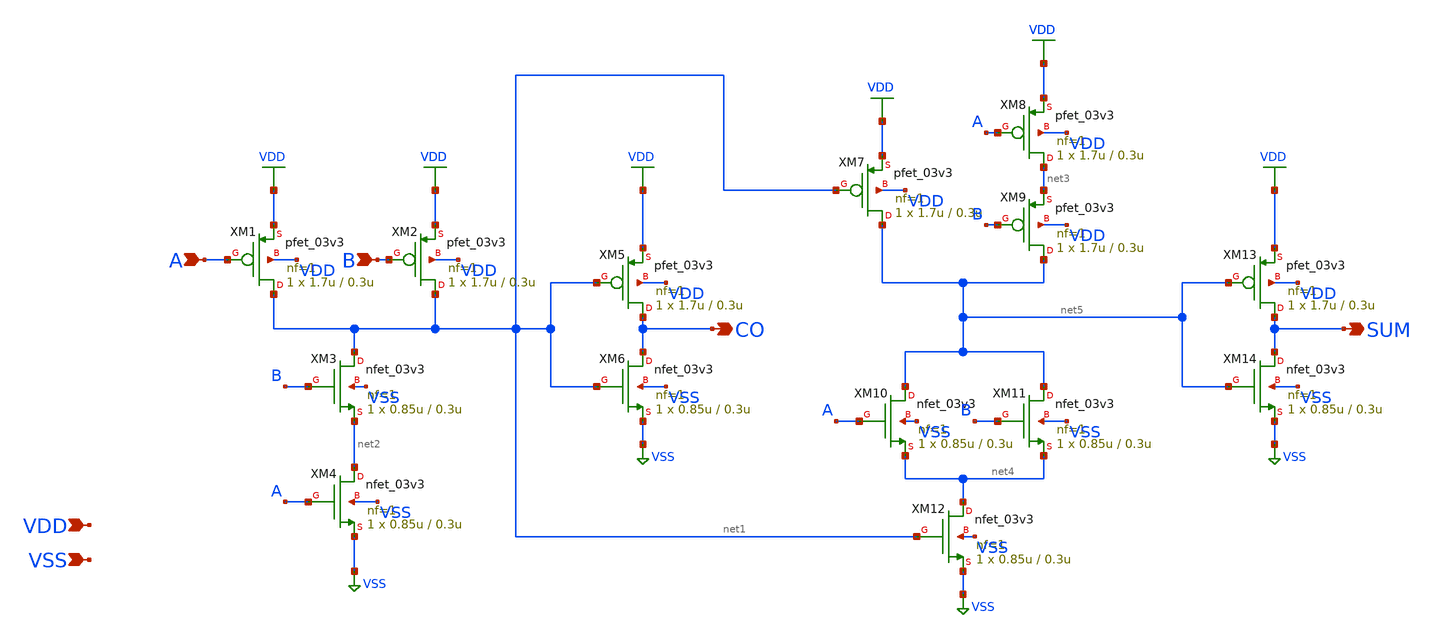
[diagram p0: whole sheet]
** sch_path: gf180mcu_osu_sc_gp9t3v3/xschem/gf180mcu_osu_sc_gp9t3v3__addh_1.sch
**.subckt gf180mcu_osu_sc_gp9t3v3__addh_1 A B SUM CO VDD VSS
*.ipin A
*.ipin B
*.opin SUM
*.opin CO
*.ipin VDD
*.ipin VSS
XM1 net1 A VDD VDD pfet_03v3 L=0.3u W=1.7u nf=1 ad='int((nf+1)/2) * W/nf * 0.18u' as='int((nf+2)/2) * W/nf * 0.18u'
+ pd='2*int((nf+1)/2) * (W/nf + 0.18u)' ps='2*int((nf+2)/2) * (W/nf + 0.18u)' nrd='0.18u / W' nrs='0.18u / W'
+ sa=0 sb=0 sd=0 m=1
XM2 net1 B VDD VDD pfet_03v3 L=0.3u W=1.7u nf=1 ad='int((nf+1)/2) * W/nf * 0.18u' as='int((nf+2)/2) * W/nf * 0.18u'
+ pd='2*int((nf+1)/2) * (W/nf + 0.18u)' ps='2*int((nf+2)/2) * (W/nf + 0.18u)' nrd='0.18u / W' nrs='0.18u / W'
+ sa=0 sb=0 sd=0 m=1
XM3 net1 B net2 VSS nfet_03v3 L=0.3u W=0.85u nf=1 ad='int((nf+1)/2) * W/nf * 0.18u' as='int((nf+2)/2) * W/nf * 0.18u'
+ pd='2*int((nf+1)/2) * (W/nf + 0.18u)' ps='2*int((nf+2)/2) * (W/nf + 0.18u)' nrd='0.18u / W' nrs='0.18u / W'
+ sa=0 sb=0 sd=0 m=1
XM4 net2 A VSS VSS nfet_03v3 L=0.3u W=0.85u nf=1 ad='int((nf+1)/2) * W/nf * 0.18u' as='int((nf+2)/2) * W/nf * 0.18u'
+ pd='2*int((nf+1)/2) * (W/nf + 0.18u)' ps='2*int((nf+2)/2) * (W/nf + 0.18u)' nrd='0.18u / W' nrs='0.18u / W'
+ sa=0 sb=0 sd=0 m=1
XM5 CO net1 VDD VDD pfet_03v3 L=0.3u W=1.7u nf=1 ad='int((nf+1)/2) * W/nf * 0.18u' as='int((nf+2)/2) * W/nf * 0.18u'
+ pd='2*int((nf+1)/2) * (W/nf + 0.18u)' ps='2*int((nf+2)/2) * (W/nf + 0.18u)' nrd='0.18u / W' nrs='0.18u / W'
+ sa=0 sb=0 sd=0 m=1
XM6 CO net1 VSS VSS nfet_03v3 L=0.3u W=0.85u nf=1 ad='int((nf+1)/2) * W/nf * 0.18u' as='int((nf+2)/2) * W/nf * 0.18u'
+ pd='2*int((nf+1)/2) * (W/nf + 0.18u)' ps='2*int((nf+2)/2) * (W/nf + 0.18u)' nrd='0.18u / W' nrs='0.18u / W'
+ sa=0 sb=0 sd=0 m=1
XM7 net5 net1 VDD VDD pfet_03v3 L=0.3u W=1.7u nf=1 ad='int((nf+1)/2) * W/nf * 0.18u' as='int((nf+2)/2) * W/nf * 0.18u'
+ pd='2*int((nf+1)/2) * (W/nf + 0.18u)' ps='2*int((nf+2)/2) * (W/nf + 0.18u)' nrd='0.18u / W' nrs='0.18u / W'
+ sa=0 sb=0 sd=0 m=1
XM8 net3 A VDD VDD pfet_03v3 L=0.3u W=1.7u nf=1 ad='int((nf+1)/2) * W/nf * 0.18u' as='int((nf+2)/2) * W/nf * 0.18u'
+ pd='2*int((nf+1)/2) * (W/nf + 0.18u)' ps='2*int((nf+2)/2) * (W/nf + 0.18u)' nrd='0.18u / W' nrs='0.18u / W'
+ sa=0 sb=0 sd=0 m=1
XM9 net5 B net3 VDD pfet_03v3 L=0.3u W=1.7u nf=1 ad='int((nf+1)/2) * W/nf * 0.18u' as='int((nf+2)/2) * W/nf * 0.18u'
+ pd='2*int((nf+1)/2) * (W/nf + 0.18u)' ps='2*int((nf+2)/2) * (W/nf + 0.18u)' nrd='0.18u / W' nrs='0.18u / W'
+ sa=0 sb=0 sd=0 m=1
XM10 net5 A net4 VSS nfet_03v3 L=0.3u W=0.85u nf=1 ad='int((nf+1)/2) * W/nf * 0.18u' as='int((nf+2)/2) * W/nf * 0.18u'
+ pd='2*int((nf+1)/2) * (W/nf + 0.18u)' ps='2*int((nf+2)/2) * (W/nf + 0.18u)' nrd='0.18u / W' nrs='0.18u / W'
+ sa=0 sb=0 sd=0 m=1
XM11 net5 B net4 VSS nfet_03v3 L=0.3u W=0.85u nf=1 ad='int((nf+1)/2) * W/nf * 0.18u' as='int((nf+2)/2) * W/nf * 0.18u'
+ pd='2*int((nf+1)/2) * (W/nf + 0.18u)' ps='2*int((nf+2)/2) * (W/nf + 0.18u)' nrd='0.18u / W' nrs='0.18u / W'
+ sa=0 sb=0 sd=0 m=1
XM12 net4 net1 VSS VSS nfet_03v3 L=0.3u W=0.85u nf=1 ad='int((nf+1)/2) * W/nf * 0.18u' as='int((nf+2)/2) * W/nf * 0.18u'
+ pd='2*int((nf+1)/2) * (W/nf + 0.18u)' ps='2*int((nf+2)/2) * (W/nf + 0.18u)' nrd='0.18u / W' nrs='0.18u / W'
+ sa=0 sb=0 sd=0 m=1
XM13 SUM net5 VDD VDD pfet_03v3 L=0.3u W=1.7u nf=1 ad='int((nf+1)/2) * W/nf * 0.18u' as='int((nf+2)/2) * W/nf * 0.18u'
+ pd='2*int((nf+1)/2) * (W/nf + 0.18u)' ps='2*int((nf+2)/2) * (W/nf + 0.18u)' nrd='0.18u / W' nrs='0.18u / W'
+ sa=0 sb=0 sd=0 m=1
XM14 SUM net5 VSS VSS nfet_03v3 L=0.3u W=0.85u nf=1 ad='int((nf+1)/2) * W/nf * 0.18u' as='int((nf+2)/2) * W/nf * 0.18u'
+ pd='2*int((nf+1)/2) * (W/nf + 0.18u)' ps='2*int((nf+2)/2) * (W/nf + 0.18u)' nrd='0.18u / W' nrs='0.18u / W'
+ sa=0 sb=0 sd=0 m=1
**.ends
.GLOBAL VDD
.GLOBAL VSS
.end
